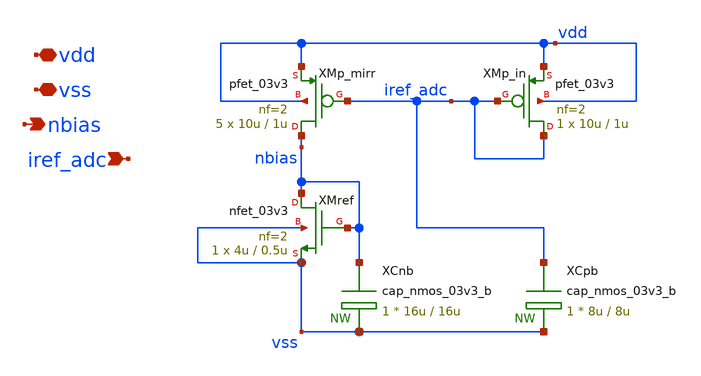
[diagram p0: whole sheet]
** sch_path: blocks/adc/comp-array/bias.sch
**.subckt bias vdd vss nbias iref_adc
*.iopin vdd
*.iopin vss
*.opin nbias
*.ipin iref_adc
XMp_in iref_adc iref_adc vdd vdd pfet_03v3 L=1u W=10u nf=2 ad='int((nf+1)/2) * W/nf * 0.18u' as='int((nf+2)/2) * W/nf * 0.18u'
+ pd='2*int((nf+1)/2) * (W/nf + 0.18u)' ps='2*int((nf+2)/2) * (W/nf + 0.18u)' nrd='0.18u / W' nrs='0.18u / W'
+ sa=0 sb=0 sd=0 m=1
XMp_mirr nbias iref_adc vdd vdd pfet_03v3 L=1u W=10u nf=2 ad='int((nf+1)/2) * W/nf * 0.18u' as='int((nf+2)/2) * W/nf * 0.18u'
+ pd='2*int((nf+1)/2) * (W/nf + 0.18u)' ps='2*int((nf+2)/2) * (W/nf + 0.18u)' nrd='0.18u / W' nrs='0.18u / W'
+ sa=0 sb=0 sd=0 m=5
XMref nbias nbias vss vss nfet_03v3 L=0.5u W=4u nf=2 ad='int((nf+1)/2) * W/nf * 0.18u' as='int((nf+2)/2) * W/nf * 0.18u'
+ pd='2*int((nf+1)/2) * (W/nf + 0.18u)' ps='2*int((nf+2)/2) * (W/nf + 0.18u)' nrd='0.18u / W' nrs='0.18u / W'
+ sa=0 sb=0 sd=0 m=1
XCnb nbias vss cap_nmos_03v3_b c_width=16u c_length=16u m=1
XCpb iref_adc vss cap_nmos_03v3_b c_width=8u c_length=8u m=1
**.ends
.end
